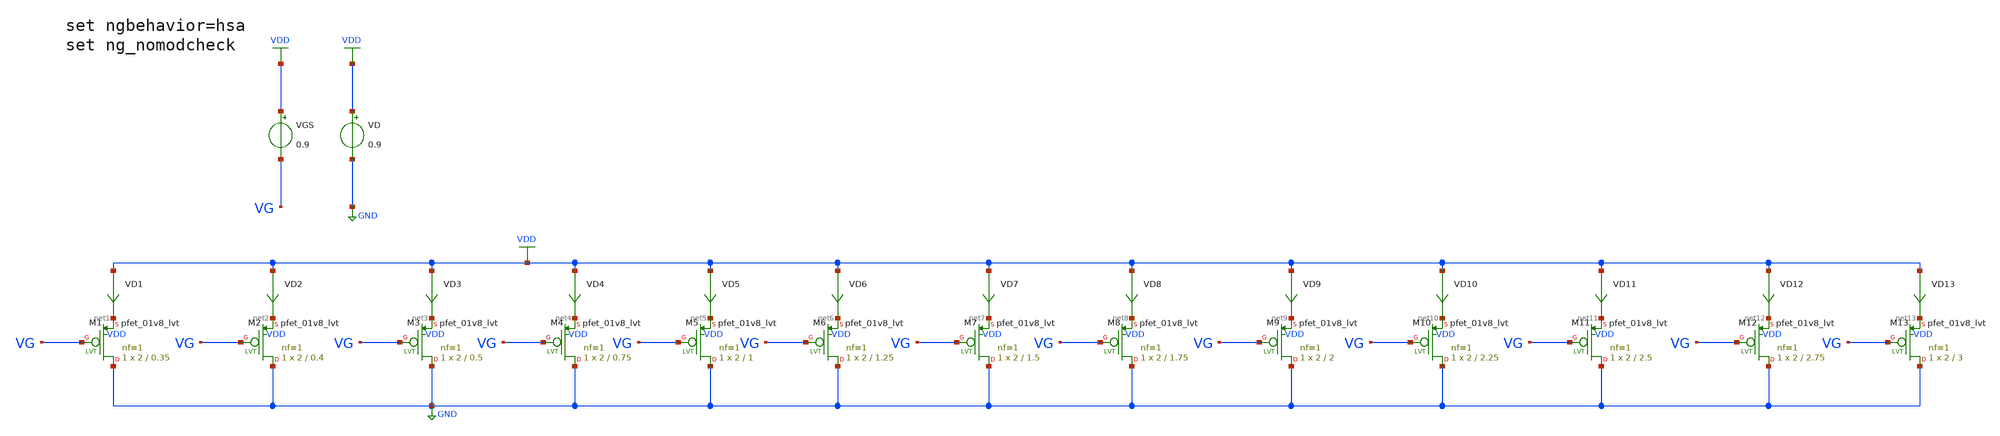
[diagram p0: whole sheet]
** sch_path: Design-Files/gmid_pmos_1v8_lvt_tb.sch
**.subckt gmid_pmos_1v8_lvt_tb
VGS VDD VG 0.9
VD VDD GND 0.9
VD1 VDD net1 0
.save i(vd1)
VD2 VDD net2 0
.save i(vd2)
VD3 VDD net3 0
.save i(vd3)
VD4 VDD net4 0
.save i(vd4)
VD5 VDD net5 0
.save i(vd5)
VD6 VDD net6 0
.save i(vd6)
VD7 VDD net7 0
.save i(vd7)
VD8 VDD net8 0
.save i(vd8)
VD9 VDD net9 0
.save i(vd9)
VD10 VDD net10 0
.save i(vd10)
VD11 VDD net11 0
.save i(vd11)
VD12 VDD net12 0
.save i(vd12)
VD13 VDD net13 0
.save i(vd13)
XM1 GND VG net1 VDD sky130_fd_pr__pfet_01v8_lvt L=0.35 W=2 nf=1 ad='int((nf+1)/2) * W/nf * 0.29' as='int((nf+2)/2) * W/nf * 0.29'
+ pd='2*int((nf+1)/2) * (W/nf + 0.29)' ps='2*int((nf+2)/2) * (W/nf + 0.29)' nrd='0.29 / W' nrs='0.29 / W'
+ sa=0 sb=0 sd=0 mult=1 m=1
XM2 GND VG net2 VDD sky130_fd_pr__pfet_01v8_lvt L=0.4 W=2 nf=1 ad='int((nf+1)/2) * W/nf * 0.29' as='int((nf+2)/2) * W/nf * 0.29'
+ pd='2*int((nf+1)/2) * (W/nf + 0.29)' ps='2*int((nf+2)/2) * (W/nf + 0.29)' nrd='0.29 / W' nrs='0.29 / W'
+ sa=0 sb=0 sd=0 mult=1 m=1
XM3 GND VG net3 VDD sky130_fd_pr__pfet_01v8_lvt L=0.5 W=2 nf=1 ad='int((nf+1)/2) * W/nf * 0.29' as='int((nf+2)/2) * W/nf * 0.29'
+ pd='2*int((nf+1)/2) * (W/nf + 0.29)' ps='2*int((nf+2)/2) * (W/nf + 0.29)' nrd='0.29 / W' nrs='0.29 / W'
+ sa=0 sb=0 sd=0 mult=1 m=1
XM4 GND VG net4 VDD sky130_fd_pr__pfet_01v8_lvt L=0.75 W=2 nf=1 ad='int((nf+1)/2) * W/nf * 0.29' as='int((nf+2)/2) * W/nf * 0.29'
+ pd='2*int((nf+1)/2) * (W/nf + 0.29)' ps='2*int((nf+2)/2) * (W/nf + 0.29)' nrd='0.29 / W' nrs='0.29 / W'
+ sa=0 sb=0 sd=0 mult=1 m=1
XM5 GND VG net5 VDD sky130_fd_pr__pfet_01v8_lvt L=1 W=2 nf=1 ad='int((nf+1)/2) * W/nf * 0.29' as='int((nf+2)/2) * W/nf * 0.29'
+ pd='2*int((nf+1)/2) * (W/nf + 0.29)' ps='2*int((nf+2)/2) * (W/nf + 0.29)' nrd='0.29 / W' nrs='0.29 / W'
+ sa=0 sb=0 sd=0 mult=1 m=1
XM6 GND VG net6 VDD sky130_fd_pr__pfet_01v8_lvt L=1.25 W=2 nf=1 ad='int((nf+1)/2) * W/nf * 0.29' as='int((nf+2)/2) * W/nf * 0.29'
+ pd='2*int((nf+1)/2) * (W/nf + 0.29)' ps='2*int((nf+2)/2) * (W/nf + 0.29)' nrd='0.29 / W' nrs='0.29 / W'
+ sa=0 sb=0 sd=0 mult=1 m=1
XM7 GND VG net7 VDD sky130_fd_pr__pfet_01v8_lvt L=1.5 W=2 nf=1 ad='int((nf+1)/2) * W/nf * 0.29' as='int((nf+2)/2) * W/nf * 0.29'
+ pd='2*int((nf+1)/2) * (W/nf + 0.29)' ps='2*int((nf+2)/2) * (W/nf + 0.29)' nrd='0.29 / W' nrs='0.29 / W'
+ sa=0 sb=0 sd=0 mult=1 m=1
XM8 GND VG net8 VDD sky130_fd_pr__pfet_01v8_lvt L=1.75 W=2 nf=1 ad='int((nf+1)/2) * W/nf * 0.29' as='int((nf+2)/2) * W/nf * 0.29'
+ pd='2*int((nf+1)/2) * (W/nf + 0.29)' ps='2*int((nf+2)/2) * (W/nf + 0.29)' nrd='0.29 / W' nrs='0.29 / W'
+ sa=0 sb=0 sd=0 mult=1 m=1
XM9 GND VG net9 VDD sky130_fd_pr__pfet_01v8_lvt L=2 W=2 nf=1 ad='int((nf+1)/2) * W/nf * 0.29' as='int((nf+2)/2) * W/nf * 0.29'
+ pd='2*int((nf+1)/2) * (W/nf + 0.29)' ps='2*int((nf+2)/2) * (W/nf + 0.29)' nrd='0.29 / W' nrs='0.29 / W'
+ sa=0 sb=0 sd=0 mult=1 m=1
XM10 GND VG net10 VDD sky130_fd_pr__pfet_01v8_lvt L=2.25 W=2 nf=1 ad='int((nf+1)/2) * W/nf * 0.29' as='int((nf+2)/2) * W/nf * 0.29'
+ pd='2*int((nf+1)/2) * (W/nf + 0.29)' ps='2*int((nf+2)/2) * (W/nf + 0.29)' nrd='0.29 / W' nrs='0.29 / W'
+ sa=0 sb=0 sd=0 mult=1 m=1
XM11 GND VG net11 VDD sky130_fd_pr__pfet_01v8_lvt L=2.5 W=2 nf=1 ad='int((nf+1)/2) * W/nf * 0.29' as='int((nf+2)/2) * W/nf * 0.29'
+ pd='2*int((nf+1)/2) * (W/nf + 0.29)' ps='2*int((nf+2)/2) * (W/nf + 0.29)' nrd='0.29 / W' nrs='0.29 / W'
+ sa=0 sb=0 sd=0 mult=1 m=1
XM12 GND VG net12 VDD sky130_fd_pr__pfet_01v8_lvt L=2.75 W=2 nf=1 ad='int((nf+1)/2) * W/nf * 0.29' as='int((nf+2)/2) * W/nf * 0.29'
+ pd='2*int((nf+1)/2) * (W/nf + 0.29)' ps='2*int((nf+2)/2) * (W/nf + 0.29)' nrd='0.29 / W' nrs='0.29 / W'
+ sa=0 sb=0 sd=0 mult=1 m=1
XM13 GND VG net13 VDD sky130_fd_pr__pfet_01v8_lvt L=3 W=2 nf=1 ad='int((nf+1)/2) * W/nf * 0.29' as='int((nf+2)/2) * W/nf * 0.29'
+ pd='2*int((nf+1)/2) * (W/nf + 0.29)' ps='2*int((nf+2)/2) * (W/nf + 0.29)' nrd='0.29 / W' nrs='0.29 / W'
+ sa=0 sb=0 sd=0 mult=1 m=1
**** begin user architecture code

** opencircuitdesign pdks install
.lib $::SKYWATER_MODELS/sky130.lib.spice ff



* ngspice commands
.option wnflag=1
.option savecurrents
.control
save all
save @m.xm1.msky130_fd_pr__pfet_01v8_lvt[gm]
save @m.xm1.msky130_fd_pr__pfet_01v8_lvt[vth]
save @m.xm1.msky130_fd_pr__pfet_01v8_lvt[gds]
save @m.xm1.msky130_fd_pr__pfet_01v8_lvt[cgg]
save @m.xm1.msky130_fd_pr__pfet_01v8_lvt[cgs]
save @m.xm1.msky130_fd_pr__pfet_01v8_lvt[cgd]
save @m.xm2.msky130_fd_pr__pfet_01v8_lvt[gm]
save @m.xm2.msky130_fd_pr__pfet_01v8_lvt[vth]
save @m.xm2.msky130_fd_pr__pfet_01v8_lvt[gds]
save @m.xm2.msky130_fd_pr__pfet_01v8_lvt[cgg]
save @m.xm2.msky130_fd_pr__pfet_01v8_lvt[cgs]
save @m.xm2.msky130_fd_pr__pfet_01v8_lvt[cgd]
save @m.xm3.msky130_fd_pr__pfet_01v8_lvt[gm]
save @m.xm3.msky130_fd_pr__pfet_01v8_lvt[vth]
save @m.xm3.msky130_fd_pr__pfet_01v8_lvt[gds]
save @m.xm3.msky130_fd_pr__pfet_01v8_lvt[cgg]
save @m.xm3.msky130_fd_pr__pfet_01v8_lvt[cgs]
save @m.xm3.msky130_fd_pr__pfet_01v8_lvt[cgd]
save @m.xm4.msky130_fd_pr__pfet_01v8_lvt[gm]
save @m.xm4.msky130_fd_pr__pfet_01v8_lvt[vth]
save @m.xm4.msky130_fd_pr__pfet_01v8_lvt[gds]
save @m.xm4.msky130_fd_pr__pfet_01v8_lvt[cgg]
save @m.xm4.msky130_fd_pr__pfet_01v8_lvt[cgs]
save @m.xm4.msky130_fd_pr__pfet_01v8_lvt[cgd]
save @m.xm5.msky130_fd_pr__pfet_01v8_lvt[gm]
save @m.xm5.msky130_fd_pr__pfet_01v8_lvt[vth]
save @m.xm5.msky130_fd_pr__pfet_01v8_lvt[gds]
save @m.xm5.msky130_fd_pr__pfet_01v8_lvt[cgg]
save @m.xm5.msky130_fd_pr__pfet_01v8_lvt[cgs]
save @m.xm5.msky130_fd_pr__pfet_01v8_lvt[cgd]
save @m.xm6.msky130_fd_pr__pfet_01v8_lvt[gm]
save @m.xm6.msky130_fd_pr__pfet_01v8_lvt[vth]
save @m.xm6.msky130_fd_pr__pfet_01v8_lvt[gds]
save @m.xm6.msky130_fd_pr__pfet_01v8_lvt[cgg]
save @m.xm6.msky130_fd_pr__pfet_01v8_lvt[cgs]
save @m.xm6.msky130_fd_pr__pfet_01v8_lvt[cgd]
save @m.xm7.msky130_fd_pr__pfet_01v8_lvt[gm]
save @m.xm7.msky130_fd_pr__pfet_01v8_lvt[vth]
save @m.xm7.msky130_fd_pr__pfet_01v8_lvt[gds]
save @m.xm7.msky130_fd_pr__pfet_01v8_lvt[cgg]
save @m.xm7.msky130_fd_pr__pfet_01v8_lvt[cgs]
save @m.xm7.msky130_fd_pr__pfet_01v8_lvt[cgd]
save @m.xm8.msky130_fd_pr__pfet_01v8_lvt[gm]
save @m.xm8.msky130_fd_pr__pfet_01v8_lvt[vth]
save @m.xm8.msky130_fd_pr__pfet_01v8_lvt[gds]
save @m.xm8.msky130_fd_pr__pfet_01v8_lvt[cgg]
save @m.xm8.msky130_fd_pr__pfet_01v8_lvt[cgs]
save @m.xm8.msky130_fd_pr__pfet_01v8_lvt[cgd]
save @m.xm9.msky130_fd_pr__pfet_01v8_lvt[gm]
save @m.xm9.msky130_fd_pr__pfet_01v8_lvt[vth]
save @m.xm9.msky130_fd_pr__pfet_01v8_lvt[gds]
save @m.xm9.msky130_fd_pr__pfet_01v8_lvt[cgg]
save @m.xm9.msky130_fd_pr__pfet_01v8_lvt[cgs]
save @m.xm9.msky130_fd_pr__pfet_01v8_lvt[cgd]
save @m.xm10.msky130_fd_pr__pfet_01v8_lvt[gm]
save @m.xm10.msky130_fd_pr__pfet_01v8_lvt[vth]
save @m.xm10.msky130_fd_pr__pfet_01v8_lvt[gds]
save @m.xm10.msky130_fd_pr__pfet_01v8_lvt[cgg]
save @m.xm10.msky130_fd_pr__pfet_01v8_lvt[cgs]
save @m.xm10.msky130_fd_pr__pfet_01v8_lvt[cgd]
save @m.xm11.msky130_fd_pr__pfet_01v8_lvt[gm]
save @m.xm11.msky130_fd_pr__pfet_01v8_lvt[vth]
save @m.xm11.msky130_fd_pr__pfet_01v8_lvt[gds]
save @m.xm11.msky130_fd_pr__pfet_01v8_lvt[cgg]
save @m.xm11.msky130_fd_pr__pfet_01v8_lvt[cgs]
save @m.xm11.msky130_fd_pr__pfet_01v8_lvt[cgd]
save @m.xm12.msky130_fd_pr__pfet_01v8_lvt[gm]
save @m.xm12.msky130_fd_pr__pfet_01v8_lvt[vth]
save @m.xm12.msky130_fd_pr__pfet_01v8_lvt[gds]
save @m.xm12.msky130_fd_pr__pfet_01v8_lvt[cgg]
save @m.xm12.msky130_fd_pr__pfet_01v8_lvt[cgs]
save @m.xm12.msky130_fd_pr__pfet_01v8_lvt[cgd]
save @m.xm13.msky130_fd_pr__pfet_01v8_lvt[gm]
save @m.xm13.msky130_fd_pr__pfet_01v8_lvt[vth]
save @m.xm13.msky130_fd_pr__pfet_01v8_lvt[gds]
save @m.xm13.msky130_fd_pr__pfet_01v8_lvt[cgg]
save @m.xm13.msky130_fd_pr__pfet_01v8_lvt[cgs]
save @m.xm13.msky130_fd_pr__pfet_01v8_lvt[cgd]
dc VGS 0.05 1.8 0.1m
** remove zero length vectors to prevent write errors
remzerovec
write /foss/designs/PDKCHAR/gmid_pmos_lvt_tb.raw

plot @m.xm1.msky130_fd_pr__pfet_01v8_lvt[gm]
plot @m.xm2.msky130_fd_pr__pfet_01v8_lvt[gm]
plot @m.xm3.msky130_fd_pr__pfet_01v8_lvt[gm]
plot @m.xm4.msky130_fd_pr__pfet_01v8_lvt[gm]
plot @m.xm5.msky130_fd_pr__pfet_01v8_lvt[gm]
plot @m.xm6.msky130_fd_pr__pfet_01v8_lvt[gm]
plot @m.xm7.msky130_fd_pr__pfet_01v8_lvt[gm]
plot @m.xm8.msky130_fd_pr__pfet_01v8_lvt[gm]
plot @m.xm9.msky130_fd_pr__pfet_01v8_lvt[gm]
plot @m.xm10.msky130_fd_pr__pfet_01v8_lvt[gm]
plot @m.xm11.msky130_fd_pr__pfet_01v8_lvt[gm]
plot @m.xm12.msky130_fd_pr__pfet_01v8_lvt[gm]
plot @m.xm13.msky130_fd_pr__pfet_01v8_lvt[gm]

wrdata /foss/designs/PDKCHAR/gmid_pmos_1_pfet_01v8_lvt_tb.txt
+ @m.xm1.msky130_fd_pr__pfet_01v8_lvt[gm] i(VD1) @m.xm1.msky130_fd_pr__pfet_01v8_lvt[vth] @m.xm1.msky130_fd_pr__pfet_01v8_lvt[gds]
+ @m.xm1.msky130_fd_pr__pfet_01v8_lvt[cgg] @m.xm1.msky130_fd_pr__pfet_01v8_lvt[cgs] @m.xm1.msky130_fd_pr__pfet_01v8_lvt[cgd]
wrdata /foss/designs/PDKCHAR/gmid_pmos_2_pfet_01v8_lvt_tb.txt
+ @m.xm2.msky130_fd_pr__pfet_01v8_lvt[gm] i(VD2) @m.xm2.msky130_fd_pr__pfet_01v8_lvt[vth] @m.xm2.msky130_fd_pr__pfet_01v8_lvt[gds]
+ @m.xm2.msky130_fd_pr__pfet_01v8_lvt[cgg] @m.xm2.msky130_fd_pr__pfet_01v8_lvt[cgs] @m.xm2.msky130_fd_pr__pfet_01v8_lvt[cgd]
wrdata /foss/designs/PDKCHAR/gmid_pmos_3_pfet_01v8_lvt_tb.txt
+ @m.xm3.msky130_fd_pr__pfet_01v8_lvt[gm] i(VD3) @m.xm3.msky130_fd_pr__pfet_01v8_lvt[vth] @m.xm3.msky130_fd_pr__pfet_01v8_lvt[gds]
+ @m.xm3.msky130_fd_pr__pfet_01v8_lvt[cgg] @m.xm3.msky130_fd_pr__pfet_01v8_lvt[cgs] @m.xm3.msky130_fd_pr__pfet_01v8_lvt[cgd]
wrdata /foss/designs/PDKCHAR/gmid_pmos_4_pfet_01v8_lvt_tb.txt
+ @m.xm4.msky130_fd_pr__pfet_01v8_lvt[gm] i(VD4) @m.xm4.msky130_fd_pr__pfet_01v8_lvt[vth] @m.xm4.msky130_fd_pr__pfet_01v8_lvt[gds]
+ @m.xm4.msky130_fd_pr__pfet_01v8_lvt[cgg] @m.xm4.msky130_fd_pr__pfet_01v8_lvt[cgs] @m.xm4.msky130_fd_pr__pfet_01v8_lvt[cgd]
wrdata /foss/designs/PDKCHAR/gmid_pmos_5_pfet_01v8_lvt_tb.txt
+ @m.xm5.msky130_fd_pr__pfet_01v8_lvt[gm] i(VD5) @m.xm5.msky130_fd_pr__pfet_01v8_lvt[vth] @m.xm5.msky130_fd_pr__pfet_01v8_lvt[gds]
+ @m.xm5.msky130_fd_pr__pfet_01v8_lvt[cgg] @m.xm5.msky130_fd_pr__pfet_01v8_lvt[cgs] @m.xm5.msky130_fd_pr__pfet_01v8_lvt[cgd]
wrdata /foss/designs/PDKCHAR/gmid_pmos_6_pfet_01v8_lvt_tb.txt
+ @m.xm6.msky130_fd_pr__pfet_01v8_lvt[gm] i(VD6) @m.xm6.msky130_fd_pr__pfet_01v8_lvt[vth] @m.xm6.msky130_fd_pr__pfet_01v8_lvt[gds]
+ @m.xm6.msky130_fd_pr__pfet_01v8_lvt[cgg] @m.xm6.msky130_fd_pr__pfet_01v8_lvt[cgs] @m.xm6.msky130_fd_pr__pfet_01v8_lvt[cgd]
wrdata /foss/designs/PDKCHAR/gmid_pmos_7_pfet_01v8_lvt_tb.txt
+ @m.xm7.msky130_fd_pr__pfet_01v8_lvt[gm] i(VD7) @m.xm7.msky130_fd_pr__pfet_01v8_lvt[vth] @m.xm7.msky130_fd_pr__pfet_01v8_lvt[gds]
+ @m.xm7.msky130_fd_pr__pfet_01v8_lvt[cgg] @m.xm7.msky130_fd_pr__pfet_01v8_lvt[cgs] @m.xm7.msky130_fd_pr__pfet_01v8_lvt[cgd]
wrdata /foss/designs/PDKCHAR/gmid_pmos_8_pfet_01v8_lvt_tb.txt
+ @m.xm8.msky130_fd_pr__pfet_01v8_lvt[gm] i(VD8) @m.xm8.msky130_fd_pr__pfet_01v8_lvt[vth] @m.xm8.msky130_fd_pr__pfet_01v8_lvt[gds]
+ @m.xm8.msky130_fd_pr__pfet_01v8_lvt[cgg] @m.xm8.msky130_fd_pr__pfet_01v8_lvt[cgs] @m.xm8.msky130_fd_pr__pfet_01v8_lvt[cgd]
wrdata /foss/designs/PDKCHAR/gmid_pmos_9_pfet_01v8_lvt_tb.txt
+ @m.xm9.msky130_fd_pr__pfet_01v8_lvt[gm] i(VD9) @m.xm9.msky130_fd_pr__pfet_01v8_lvt[vth] @m.xm9.msky130_fd_pr__pfet_01v8_lvt[gds]
+ @m.xm9.msky130_fd_pr__pfet_01v8_lvt[cgg] @m.xm9.msky130_fd_pr__pfet_01v8_lvt[cgs] @m.xm9.msky130_fd_pr__pfet_01v8_lvt[cgd]
wrdata /foss/designs/PDKCHAR/gmid_pmos_10_pfet_01v8_lvt_tb.txt
+ @m.xm10.msky130_fd_pr__pfet_01v8_lvt[gm] i(VD10) @m.xm10.msky130_fd_pr__pfet_01v8_lvt[vth] @m.xm10.msky130_fd_pr__pfet_01v8_lvt[gds]
+ @m.xm10.msky130_fd_pr__pfet_01v8_lvt[cgg] @m.xm10.msky130_fd_pr__pfet_01v8_lvt[cgs] @m.xm10.msky130_fd_pr__pfet_01v8_lvt[cgd]
wrdata /foss/designs/PDKCHAR/gmid_pmos_11_pfet_01v8_lvt_tb.txt
+ @m.xm11.msky130_fd_pr__pfet_01v8_lvt[gm] i(VD11) @m.xm11.msky130_fd_pr__pfet_01v8_lvt[vth] @m.xm11.msky130_fd_pr__pfet_01v8_lvt[gds]
+ @m.xm11.msky130_fd_pr__pfet_01v8_lvt[cgg] @m.xm11.msky130_fd_pr__pfet_01v8_lvt[cgs] @m.xm11.msky130_fd_pr__pfet_01v8_lvt[cgd]
wrdata /foss/designs/PDKCHAR/gmid_pmos_12_pfet_01v8_lvt_tb.txt
+ @m.xm12.msky130_fd_pr__pfet_01v8_lvt[gm] i(VD12) @m.xm12.msky130_fd_pr__pfet_01v8_lvt[vth] @m.xm12.msky130_fd_pr__pfet_01v8_lvt[gds]
+ @m.xm12.msky130_fd_pr__pfet_01v8_lvt[cgg] @m.xm12.msky130_fd_pr__pfet_01v8_lvt[cgs] @m.xm12.msky130_fd_pr__pfet_01v8_lvt[cgd]
wrdata /foss/designs/PDKCHAR/gmid_pmos_13_pfet_01v8_lvt_tb.txt
+ @m.xm13.msky130_fd_pr__pfet_01v8_lvt[gm] i(VD13) @m.xm13.msky130_fd_pr__pfet_01v8_lvt[vth] @m.xm13.msky130_fd_pr__pfet_01v8_lvt[gds]
+ @m.xm13.msky130_fd_pr__pfet_01v8_lvt[cgg] @m.xm13.msky130_fd_pr__pfet_01v8_lvt[cgs] @m.xm13.msky130_fd_pr__pfet_01v8_lvt[cgd]
set appendwrite
op
remzerovec
write /foss/designs/PDKCHAR/gmid_pmos_lvt_tb.raw
quit 0
.endc


**** end user architecture code
**.ends
.GLOBAL GND
.GLOBAL VDD
.end
